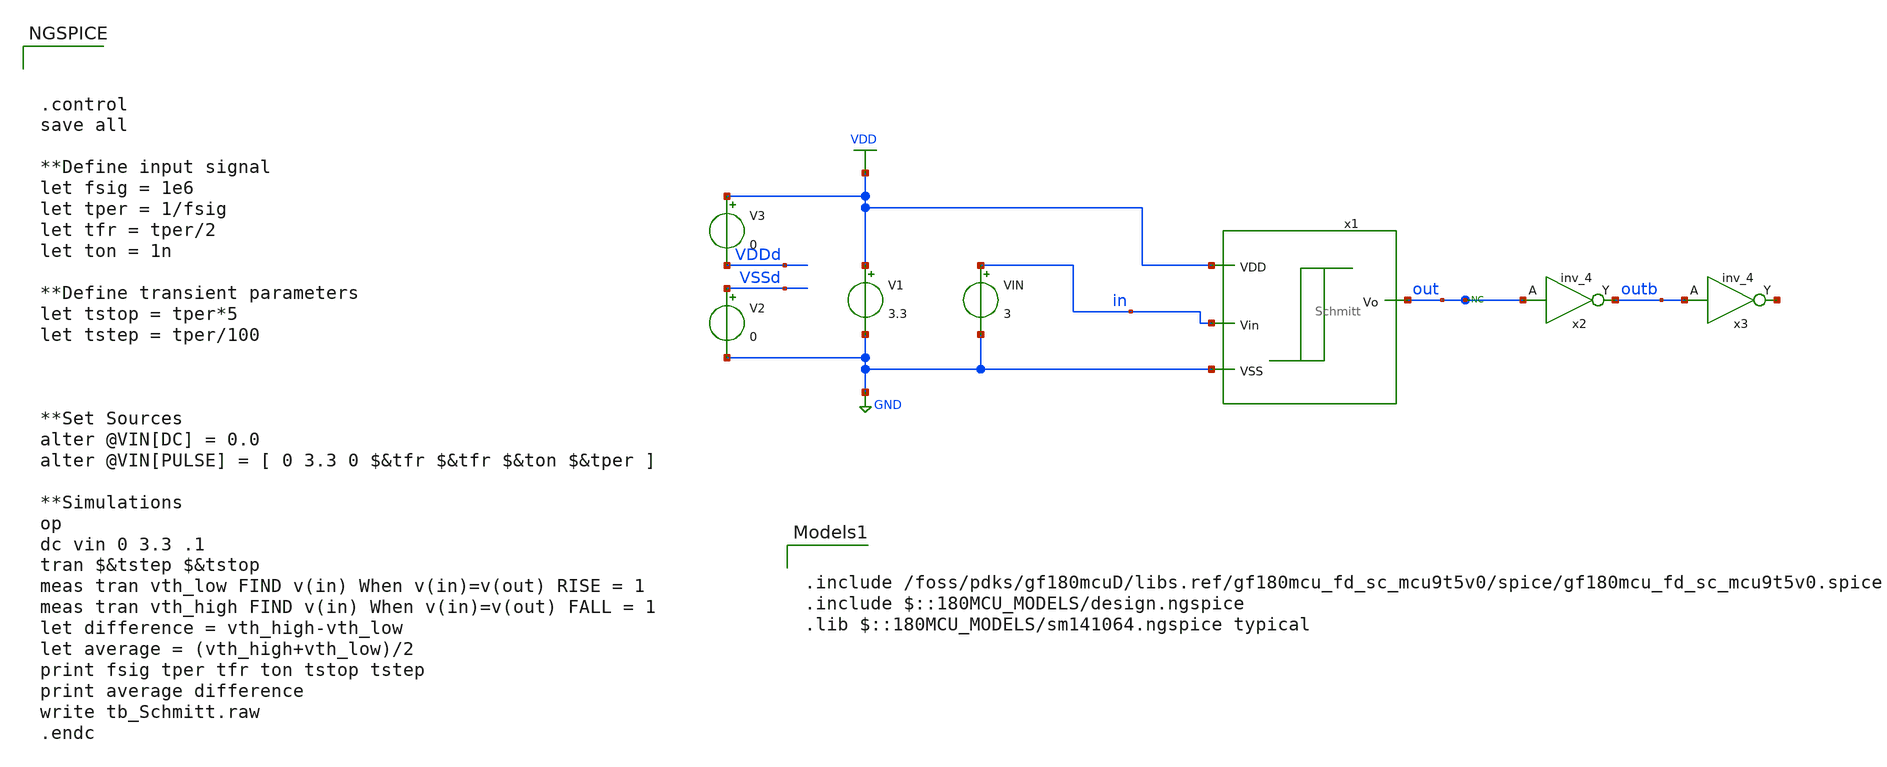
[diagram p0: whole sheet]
** sch_path: testbenches/tb_Schmitt.sch
**.subckt tb_Schmitt
x1 VDD in out GND Schmitt
V1 VDD GND 3.3
VIN in GND 3
* noconn out
x2 out outb VDDd VDDd VSSd VSSd gf180mcu_fd_sc_mcu9t5v0__inv_4
x3 outb net1 VDDd VDDd VSSd VSSd gf180mcu_fd_sc_mcu9t5v0__inv_4
V2 VSSd GND 0
V3 VDD VDDd 0
**** begin user architecture code



.control
save all

**Define input signal
let fsig = 1e6
let tper = 1/fsig
let tfr = tper/2
let ton = 1n

**Define transient parameters
let tstop = tper*5
let tstep = tper/100



**Set Sources
alter @VIN[DC] = 0.0
alter @VIN[PULSE] = [ 0 3.3 0 $&tfr $&tfr $&ton $&tper ]

**Simulations
op
dc vin 0 3.3 .1
tran $&tstep $&tstop
meas tran vth_low FIND v(in) When v(in)=v(out) RISE = 1
meas tran vth_high FIND v(in) When v(in)=v(out) FALL = 1
let difference = vth_high-vth_low
let average = (vth_high+vth_low)/2
print fsig tper tfr ton tstop tstep
print average difference
write tb_Schmitt.raw
.endc



.include /foss/pdks/gf180mcuD/libs.ref/gf180mcu_fd_sc_mcu9t5v0/spice/gf180mcu_fd_sc_mcu9t5v0.spice
.include $::180MCU_MODELS/design.ngspice
.lib $::180MCU_MODELS/sm141064.ngspice typical

**** end user architecture code
**.ends

* expanding   symbol:  switch_matrix_gf180mcu_9t5v0/Schmitt/Schmitt.sym # of pins=4
** sym_path: Schmitt/Schmitt.sym
** sch_path: Schmitt/Schmitt.sch
.subckt Schmitt VDD Vin Vo VSS
*.ipin VDD
*.ipin VSS
*.ipin Vin
*.opin Vo
XM9 schmitt Vin bot VSS nfet_06v0 L=0.70u W=2u nf=2 ad='int((nf+1)/2) * W/nf * 0.18u' as='int((nf+2)/2) * W/nf * 0.18u'
+ pd='2*int((nf+1)/2) * (W/nf + 0.18u)' ps='2*int((nf+2)/2) * (W/nf + 0.18u)' nrd='0.18u / W' nrs='0.18u / W'
+ sa=0 sb=0 sd=0 m=1
XM10 schmitt Vin top VDD pfet_06v0 L=0.55u W=6u nf=2 ad='int((nf+1)/2) * W/nf * 0.18u' as='int((nf+2)/2) * W/nf * 0.18u'
+ pd='2*int((nf+1)/2) * (W/nf + 0.18u)' ps='2*int((nf+2)/2) * (W/nf + 0.18u)' nrd='0.18u / W' nrs='0.18u / W'
+ sa=0 sb=0 sd=0 m=1
XM11 VDD schmitt bot VSS nfet_06v0 L=0.70u W=2u nf=2 ad='int((nf+1)/2) * W/nf * 0.18u' as='int((nf+2)/2) * W/nf * 0.18u'
+ pd='2*int((nf+1)/2) * (W/nf + 0.18u)' ps='2*int((nf+2)/2) * (W/nf + 0.18u)' nrd='0.18u / W' nrs='0.18u / W'
+ sa=0 sb=0 sd=0 m=1
XM12 top Vin VDD VDD pfet_06v0 L=0.55u W=6u nf=2 ad='int((nf+1)/2) * W/nf * 0.18u' as='int((nf+2)/2) * W/nf * 0.18u'
+ pd='2*int((nf+1)/2) * (W/nf + 0.18u)' ps='2*int((nf+2)/2) * (W/nf + 0.18u)' nrd='0.18u / W' nrs='0.18u / W'
+ sa=0 sb=0 sd=0 m=1
XM13 Vo schmitt VSS VSS nfet_06v0 L=0.70u W=2u nf=2 ad='int((nf+1)/2) * W/nf * 0.18u' as='int((nf+2)/2) * W/nf * 0.18u'
+ pd='2*int((nf+1)/2) * (W/nf + 0.18u)' ps='2*int((nf+2)/2) * (W/nf + 0.18u)' nrd='0.18u / W' nrs='0.18u / W'
+ sa=0 sb=0 sd=0 m=1
XM14 Vo schmitt VDD VDD pfet_06v0 L=0.55u W=6u nf=2 ad='int((nf+1)/2) * W/nf * 0.18u' as='int((nf+2)/2) * W/nf * 0.18u'
+ pd='2*int((nf+1)/2) * (W/nf + 0.18u)' ps='2*int((nf+2)/2) * (W/nf + 0.18u)' nrd='0.18u / W' nrs='0.18u / W'
+ sa=0 sb=0 sd=0 m=1
XM15 VSS schmitt top VDD pfet_06v0 L=0.55u W=6u nf=2 ad='int((nf+1)/2) * W/nf * 0.18u' as='int((nf+2)/2) * W/nf * 0.18u'
+ pd='2*int((nf+1)/2) * (W/nf + 0.18u)' ps='2*int((nf+2)/2) * (W/nf + 0.18u)' nrd='0.18u / W' nrs='0.18u / W'
+ sa=0 sb=0 sd=0 m=1
XM1 bot Vin VSS VSS nfet_06v0 L=0.70u W=2u nf=2 ad='int((nf+1)/2) * W/nf * 0.18u' as='int((nf+2)/2) * W/nf * 0.18u'
+ pd='2*int((nf+1)/2) * (W/nf + 0.18u)' ps='2*int((nf+2)/2) * (W/nf + 0.18u)' nrd='0.18u / W' nrs='0.18u / W'
+ sa=0 sb=0 sd=0 m=1
.ends

.GLOBAL GND
.GLOBAL VDD
.end
